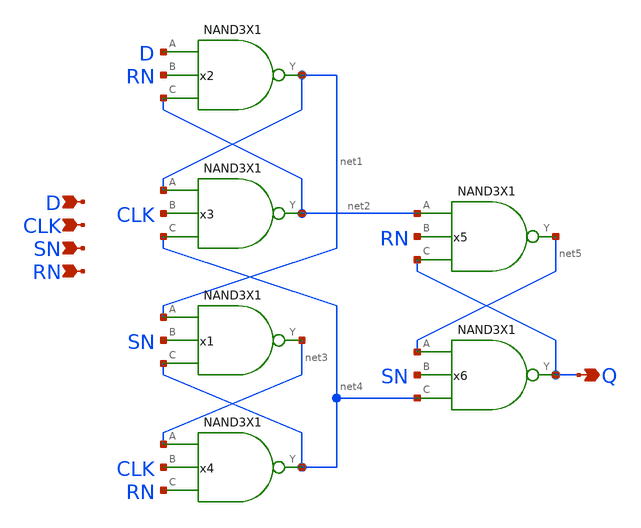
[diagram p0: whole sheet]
** sch_path: archives/lib/xschem/DFFSNRNQX1.sch
**.subckt DFFSNRNQX1 Q D CLK SN RN
*.opin Q
*.ipin D
*.ipin CLK
*.ipin SN
*.ipin RN
x1 net3 net1 SN net4 VDD VSS NAND3X1
x3 net2 net1 CLK net4 VDD VSS NAND3X1
x6 Q net5 SN net4 VDD VSS NAND3X1
x2 net1 D RN net2 VDD VSS NAND3X1
x4 net4 net3 CLK RN VDD VSS NAND3X1
x5 net5 net2 RN Q VDD VSS NAND3X1
**.ends
.end
